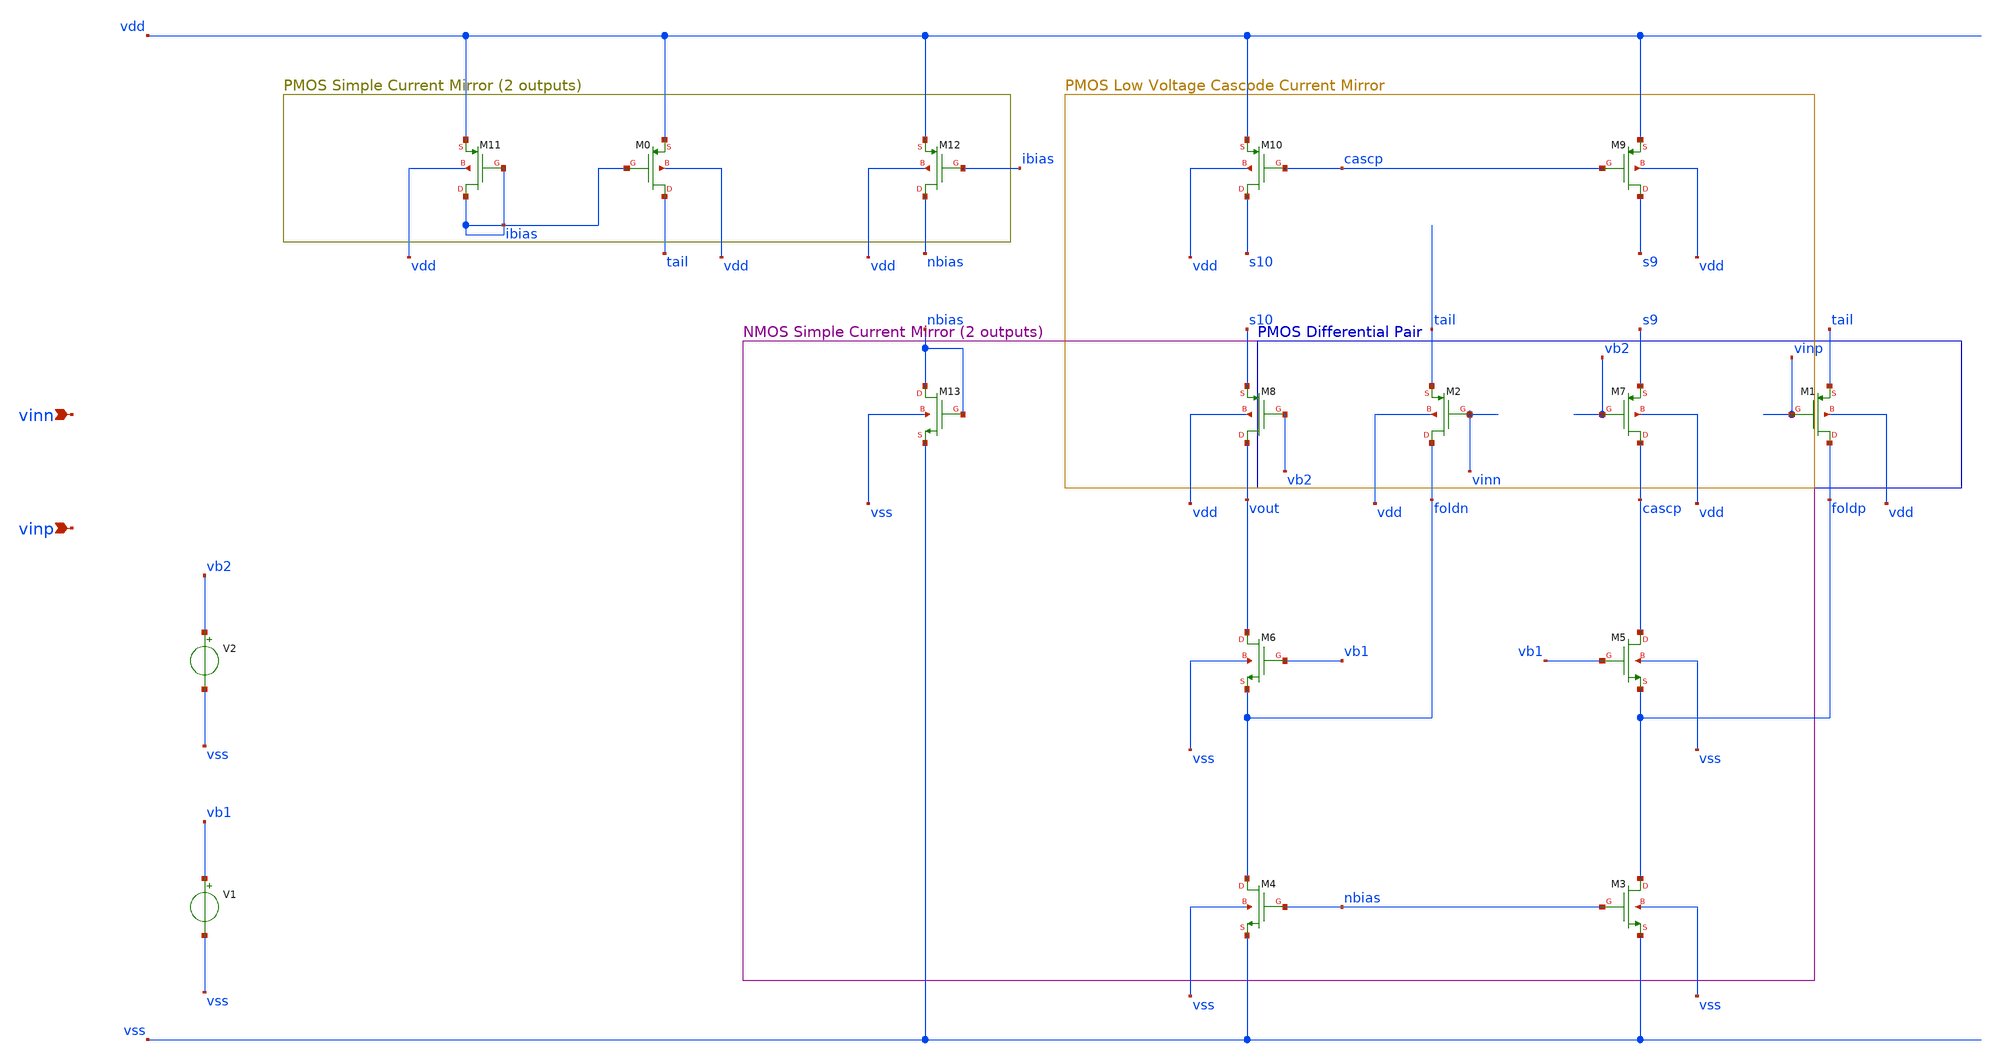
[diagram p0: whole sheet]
** sch_path: platform/packages/spicexplorer-netlist2xschem/notebooks/folded_cascode_annotated.sch
**.subckt folded_cascode_annotated vinn vinp
*.ipin vinn
*.ipin vinp
XM4 foldn nbias vss vss nmos w=x_dut_xm4_w l=x_dut_xm4_l ng=x_dut_xm4_ng m=x_dut_xm4_m
XM1 foldp vinp tail vdd pmos w=x_dut_xm1_w l=x_dut_xm1_l ng=x_dut_xm1_ng m=x_dut_xm1_m
XM2 foldn vinn tail vdd pmos w=x_dut_xm2_w l=x_dut_xm2_l ng=x_dut_xm2_ng m=x_dut_xm2_m
XM3 foldp nbias vss vss nmos w=x_dut_xm3_w l=x_dut_xm3_l ng=x_dut_xm3_ng m=x_dut_xm3_m
XM11 ibias ibias vdd vdd pmos w=x_dut_xm11_w l=x_dut_xm11_l ng=x_dut_xm11_ng m=x_dut_xm11_m
XM0 tail ibias vdd vdd pmos w=x_dut_xm0_w l=x_dut_xm0_l ng=x_dut_xm0_ng m=x_dut_xm0_m
XM6 vout vb1 foldn vss nmos w=x_dut_xm6_w l=x_dut_xm6_l ng=x_dut_xm6_ng m=x_dut_xm6_m
XM5 cascp vb1 foldp vss nmos w=x_dut_xm5_w l=x_dut_xm5_l ng=x_dut_xm5_ng m=x_dut_xm5_m
XM7 cascp vb2 s9 vdd pmos w=x_dut_xm7_w l=x_dut_xm7_l ng=x_dut_xm7_ng m=x_dut_xm7_m
XM8 vout vb2 s10 vdd pmos w=x_dut_xm8_w l=x_dut_xm8_l ng=x_dut_xm8_ng m=x_dut_xm8_m
XM9 s9 cascp vdd vdd pmos w=x_dut_xm9_w l=x_dut_xm9_l ng=x_dut_xm9_ng m=x_dut_xm9_m
XM10 s10 cascp vdd vdd pmos w=x_dut_xm10_w l=x_dut_xm10_l ng=x_dut_xm10_ng m=x_dut_xm10_m
XM12 nbias ibias vdd vdd pmos w=x_dut_xm12_w l=x_dut_xm12_l ng=x_dut_xm12_ng m=x_dut_xm12_m
XM13 nbias nbias vss vss nmos w=x_dut_xm13_w l=x_dut_xm13_l ng=x_dut_xm13_ng m=x_dut_xm13_m
V1 vb1 vss x_dut_vb1
V2 vb2 vss x_dut_vb2
**.ends
.end
